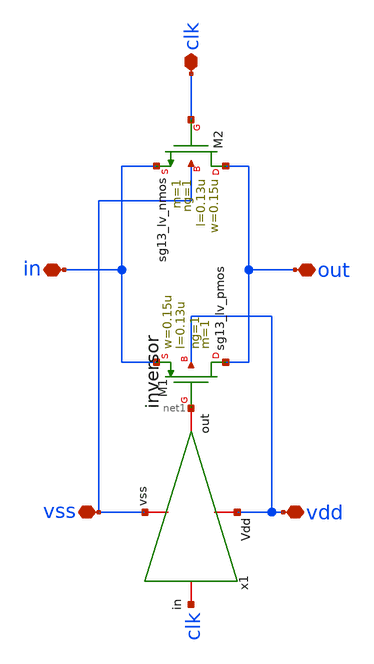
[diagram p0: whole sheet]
** sch_path: design/blocks/interruptor/interruptor.sch
**.subckt interruptor clk in out vdd vss
*.iopin clk
*.iopin in
*.iopin out
*.iopin vdd
*.iopin vss
XM1 out net1 in vdd sg13_lv_pmos w=0.15u l=0.13u ng=1 m=1 mm_ok=1
XM2 out clk in vss sg13_lv_nmos w=0.15u l=0.13u ng=1 m=1 mm_ok=1
x1 vdd net1 clk vss inversor
**.ends

* expanding   symbol:  blocks/inversor/schematic/inversor.sym # of pins=4
** sym_path: design/blocks/inversor/schematic/inversor.sym
** sch_path: design/blocks/inversor/schematic/inversor.sch
.subckt inversor Vdd out in vss
*.iopin Vdd
*.iopin out
*.iopin vss
*.iopin in
XM1 out in Vdd Vdd sg13_lv_pmos w=0.15u l=0.13u ng=1 m=1 mm_ok=1
XM2 out in vss vss sg13_lv_nmos w=0.15u l=0.13u ng=1 m=1 mm_ok=1
.ends

.end
